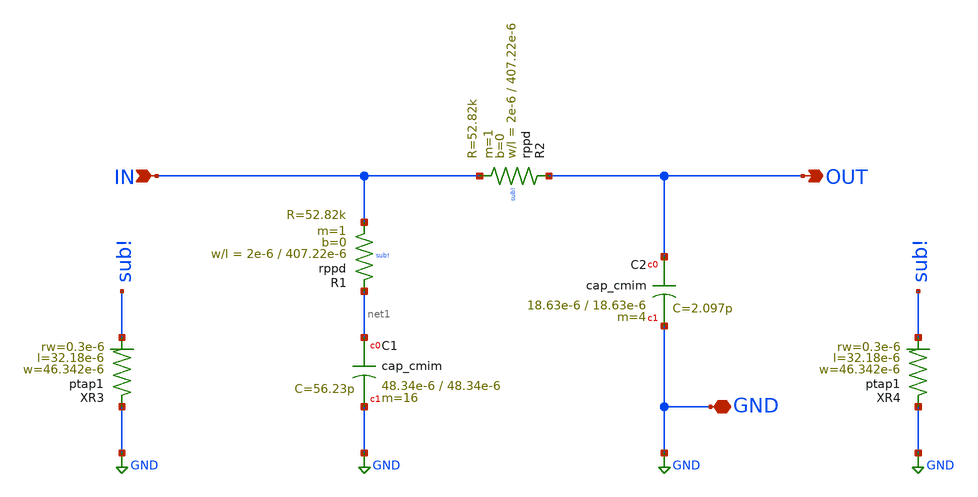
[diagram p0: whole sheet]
** sch_path: xschem/LOOP_FILTER.sch
**.subckt LOOP_FILTER OUT GND IN
*.opin OUT
*.iopin GND
*.ipin IN
XC2 OUT GND cap_cmim w=18.63e-6 l=18.63e-6 m=4 mm_ok=1
XC1 net1 GND cap_cmim w=48.34e-6 l=48.34e-6 m=16 mm_ok=1
XR2 OUT IN sub! rppd w=2e-6 l=407.22e-6 m=1 b=0 mm_ok=1
XR1 net1 IN sub! rppd w=2e-6 l=407.22e-6 m=1 b=0 mm_ok=1
XR3 GND sub! ptap1 R=1.462 w=46.342e-6 l=32.18e-6 rw=0.3e-6
XR4 GND sub! ptap1 R=1.462 w=46.342e-6 l=32.18e-6 rw=0.3e-6
**.ends
.GLOBAL GND
.end
